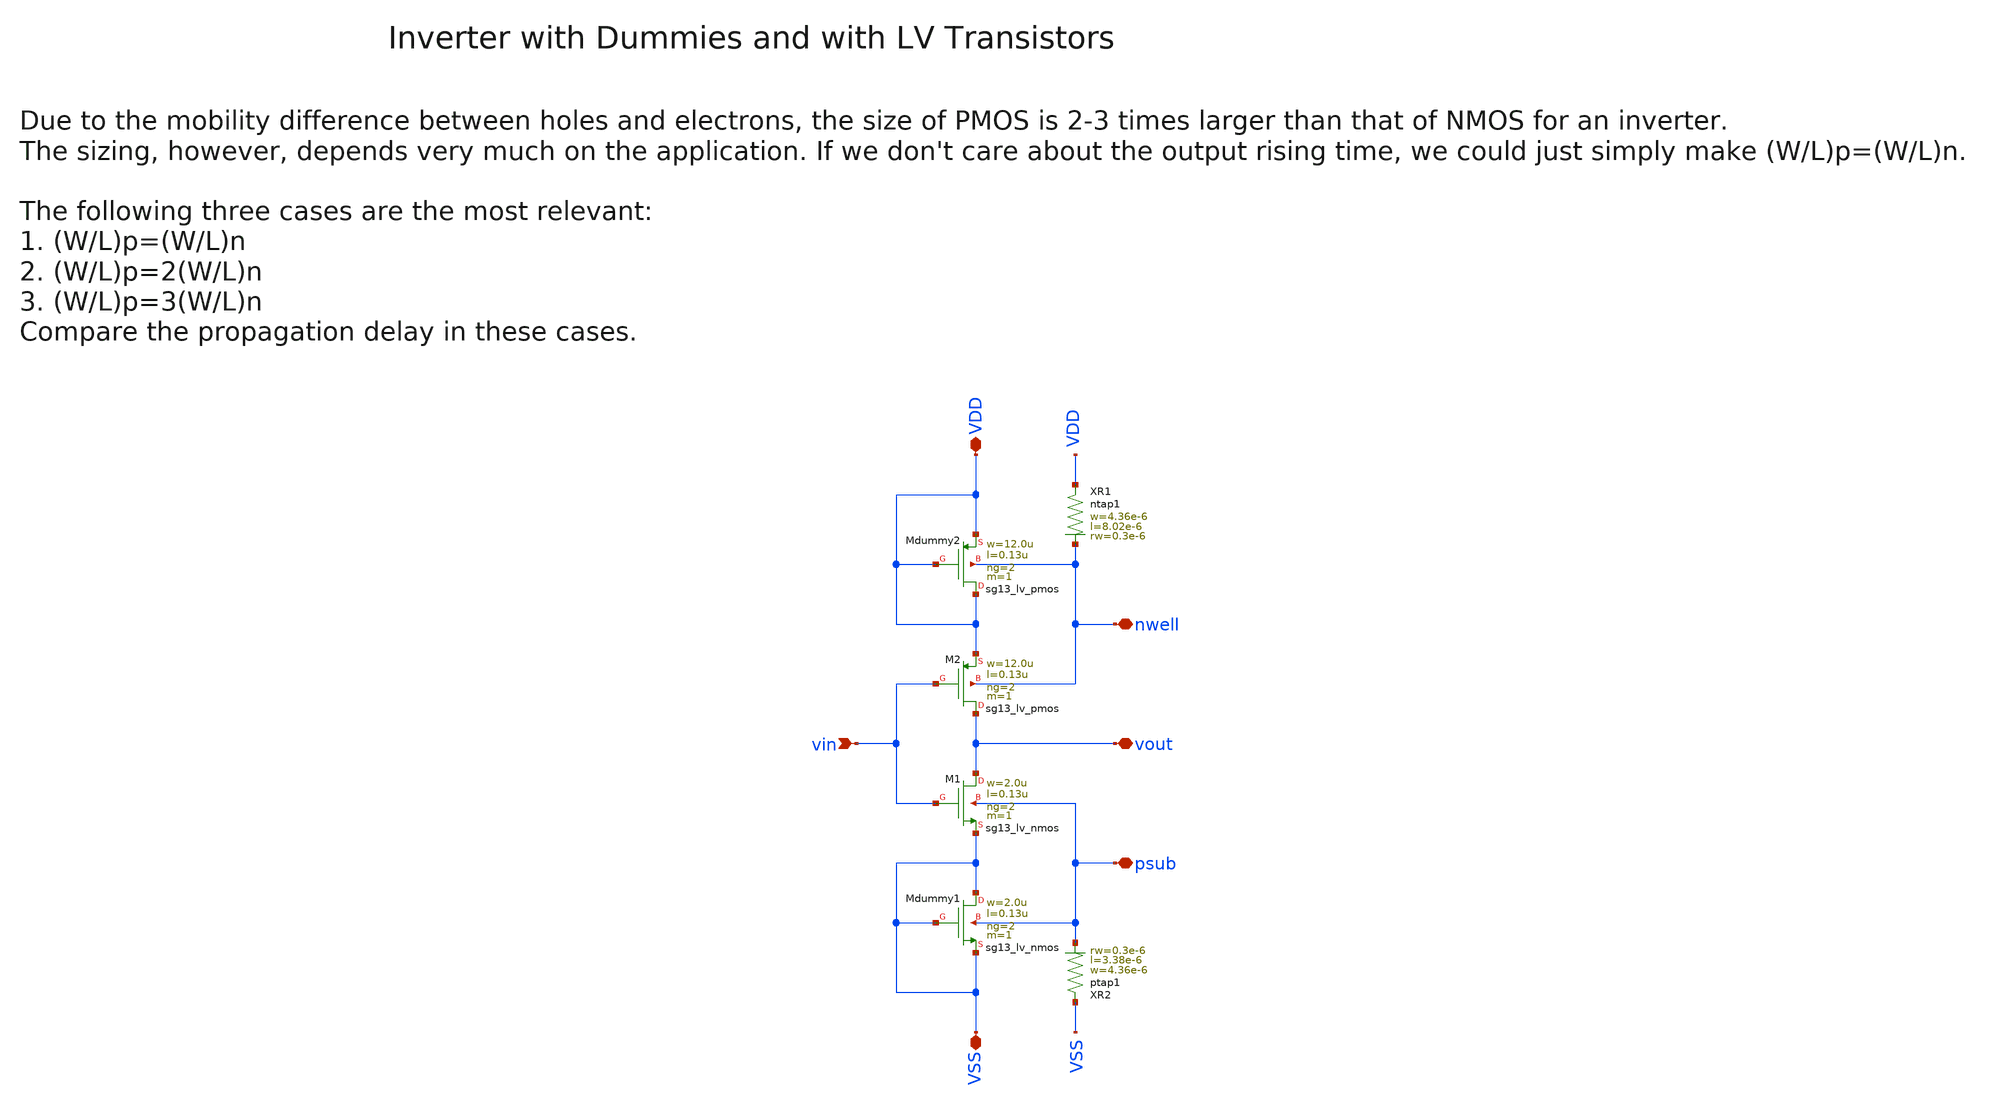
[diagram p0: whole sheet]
** sch_path: ihp130/macros/iqmod/schematic/iqmod_mfb_lpf_ota_core_spdt_switch_inv.sch
**.subckt iqmod_mfb_lpf_ota_core_spdt_switch_inv vin VDD VSS vout nwell psub
*.ipin vin
*.iopin VDD
*.iopin VSS
*.iopin vout
*.iopin nwell
*.iopin psub
XM1 vout vin VSS psub sg13_lv_nmos w=2.0u l=0.13u ng=2 m=1 mm_ok=1
XM2 vout vin VDD nwell sg13_lv_pmos w=12.0u l=0.13u ng=2 m=1 mm_ok=1
XMdummy1 VSS VSS VSS psub sg13_lv_nmos w=2.0u l=0.13u ng=2 m=1 mm_ok=1
XMdummy2 VDD VDD VDD nwell sg13_lv_pmos w=12.0u l=0.13u ng=2 m=1 mm_ok=1
XR1 VDD nwell ntap1 R=9.673 w=4.36e-6 l=8.02e-6 rw=0.3e-6
XR2 VSS psub ptap1 R=15.96 w=4.36e-6 l=3.38e-6 rw=0.3e-6
**.ends
.end
